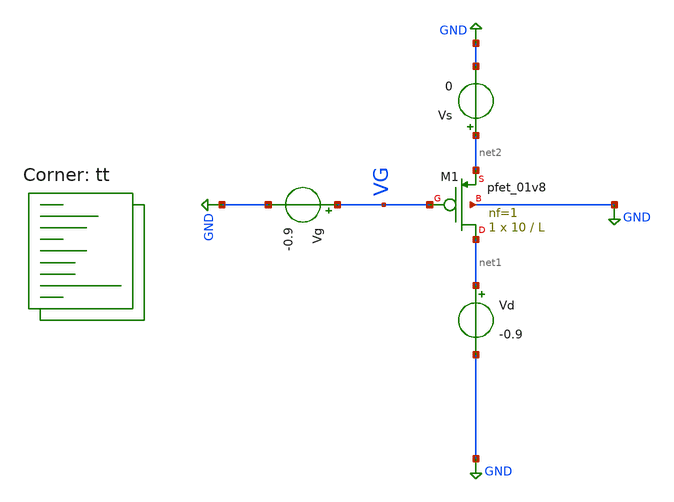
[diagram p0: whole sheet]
** sch_path: GmIdp.sch
**.subckt GmIdp
Vg VG GND -0.9
Vd net1 GND -0.9
XM1 net1 VG net2 GND sky130_fd_pr__pfet_01v8 L=L W=10 nf=1 ad='int((nf+1)/2) * W/nf * 0.29' as='int((nf+2)/2) * W/nf * 0.29'
+ pd='2*int((nf+1)/2) * (W/nf + 0.29)' ps='2*int((nf+2)/2) * (W/nf + 0.29)' nrd='0.29 / W' nrs='0.29 / W'
+ sa=0 sb=0 sd=0 mult=1 m=1
Vs net2 GND 0
**** begin user architecture code
.lib $::SKYWATER_MODELS/sky130.lib.spice tt

* this option enables mos model bin
* selection based on W/NF instead of W
.option wnflag=1
.option savecurrents
.param L=0.15
.param Vsb=0
.control
save all
save @m.xm1.msky130_fd_pr__pfet_01v8[id]
save @m.xm1.msky130_fd_pr__pfet_01v8[gm]
save @m.xm1.msky130_fd_pr__pfet_01v8[gds]
save @m.xm1.msky130_fd_pr__pfet_01v8[vth]
save @m.xm1.msky130_fd_pr__pfet_01v8[cgg]
save @m.xm1.msky130_fd_pr__pfet_01v8[vds]
save @m.xm1.msky130_fd_pr__pfet_01v8[vgs]
save @m.xm1.msky130_fd_pr__pfet_01v8[vbs]
let Lmax = 3
let Ldelta = 0.15;
let Lstart = 0.15;
let Lact = 0.15

while Lact le Lmax
  echo L = $&Lact
  dc Vs 0 -0.2 -0.02
  let Lact = Lact + Ldelta
  alterparam L=Lact
end
 plot all.@m.xm1.msky130_fd_pr__pfet_01v8[id]
 plot all.@m.xm1.msky130_fd_pr__pfet_01v8[gm]
 plot all.@m.xm1.msky130_fd_pr__pfet_01v8[gds]
 plot all.@m.xm1.msky130_fd_pr__pfet_01v8[vth]
 plot all.@m.xm1.msky130_fd_pr__pfet_01v8[cgg]
 plot all.@m.xm1.msky130_fd_pr__pfet_01v8[vbs]
 set appendwrite
 set filetype=binary
 write GmIdp.raw
 set wr_singlescale
 set wr_vecnames
 wrdata GmIdpvs.csv all.@m.xm1.msky130_fd_pr__pfet_01v8[id] all.@m.xm1.msky130_fd_pr__pfet_01v8[gm]
+ all.@m.xm1.msky130_fd_pr__pfet_01v8[gds] all.@m.xm1.msky130_fd_pr__pfet_01v8[cgg] all.@m.xm1.msky130_fd_pr__pfet_01v8[vgs]
+  all.@m.xm1.msky130_fd_pr__pfet_01v8[vds] all.@m.xm1.msky130_fd_pr__pfet_01v8[vth]
.endc


**** end user architecture code
**.ends
.GLOBAL GND
.end
